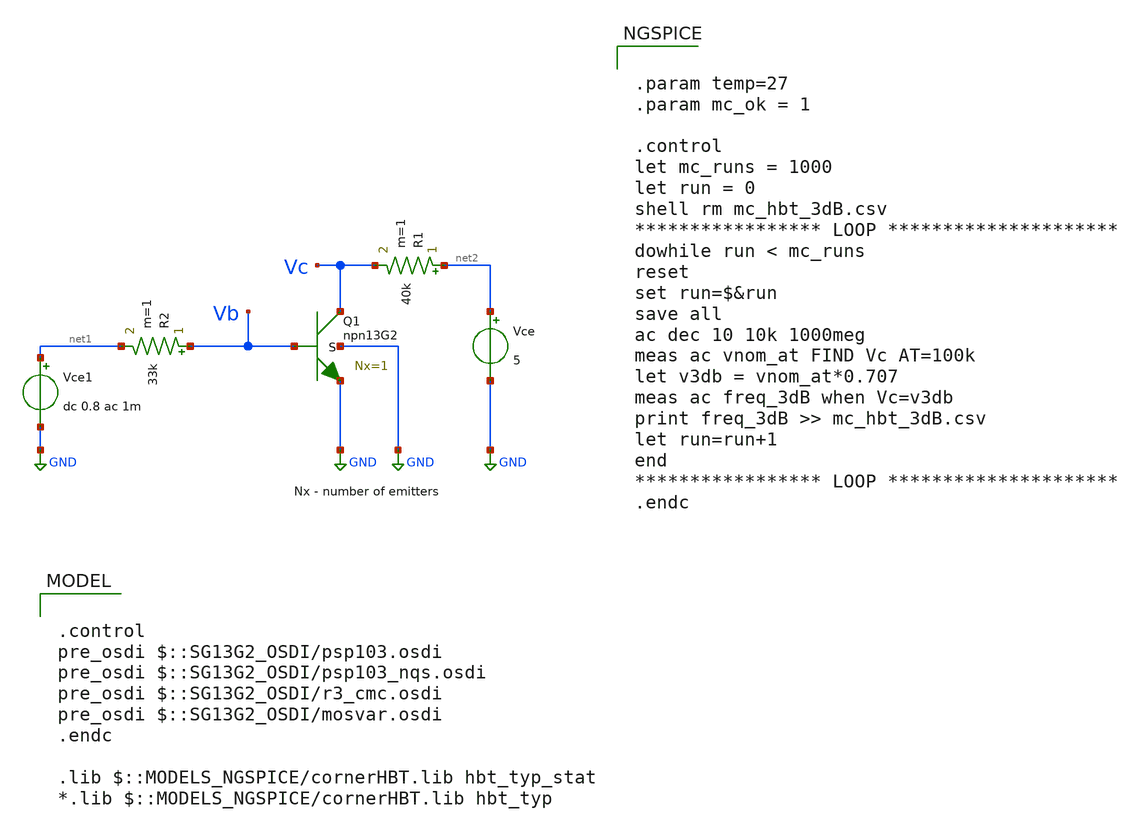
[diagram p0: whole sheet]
** sch_path: ihp-sg13g2/xschem_libs/sg13g2_tests/mc_hbt_13g2_ac/schematic/mc_hbt_13g2_ac.sch
* Copyright 2023 IHP PDK Authors
**.subckt mc_hbt_13g2_ac
Vce net2 GND 5
R1 net2 Vc 40k m=1
Vce1 net1 GND dc 0.8 ac 1m
R2 Vb net1 33k m=1
XQ1 Vc Vb GND GND npn13G2 Nx=1 mm_ok=1
**** begin user architecture code

.control
pre_osdi $::SG13G2_OSDI/psp103.osdi
pre_osdi $::SG13G2_OSDI/psp103_nqs.osdi
pre_osdi $::SG13G2_OSDI/r3_cmc.osdi
pre_osdi $::SG13G2_OSDI/mosvar.osdi
.endc

.lib $::MODELS_NGSPICE/cornerHBT.lib hbt_typ_stat
*.lib $::MODELS_NGSPICE/cornerHBT.lib hbt_typ



.param temp=27
.param mc_ok = 1

.control
let mc_runs = 1000
let run = 0
shell rm mc_hbt_3dB.csv
***************** LOOP *********************
dowhile run < mc_runs
reset
set run=$&run
save all
ac dec 10 10k 1000meg
meas ac vnom_at FIND Vc AT=100k
let v3db = vnom_at*0.707
meas ac freq_3dB when Vc=v3db
print freq_3dB >> mc_hbt_3dB.csv
let run=run+1
end
***************** LOOP *********************
.endc


**** end user architecture code
**.ends
.GLOBAL GND
.end
